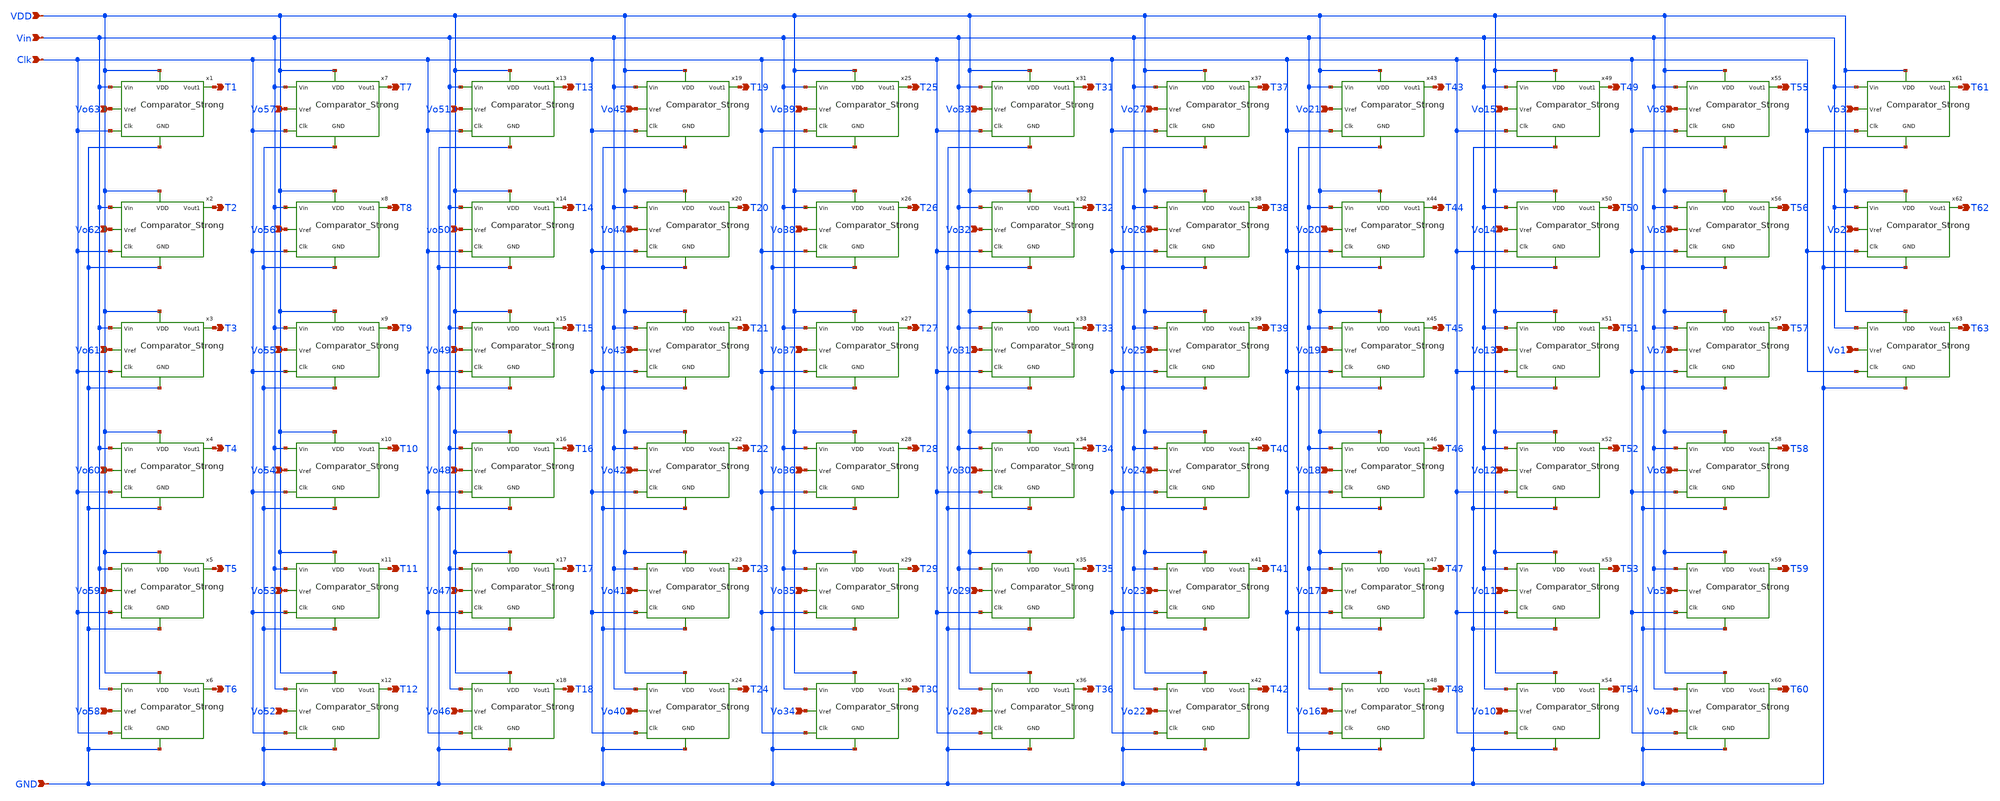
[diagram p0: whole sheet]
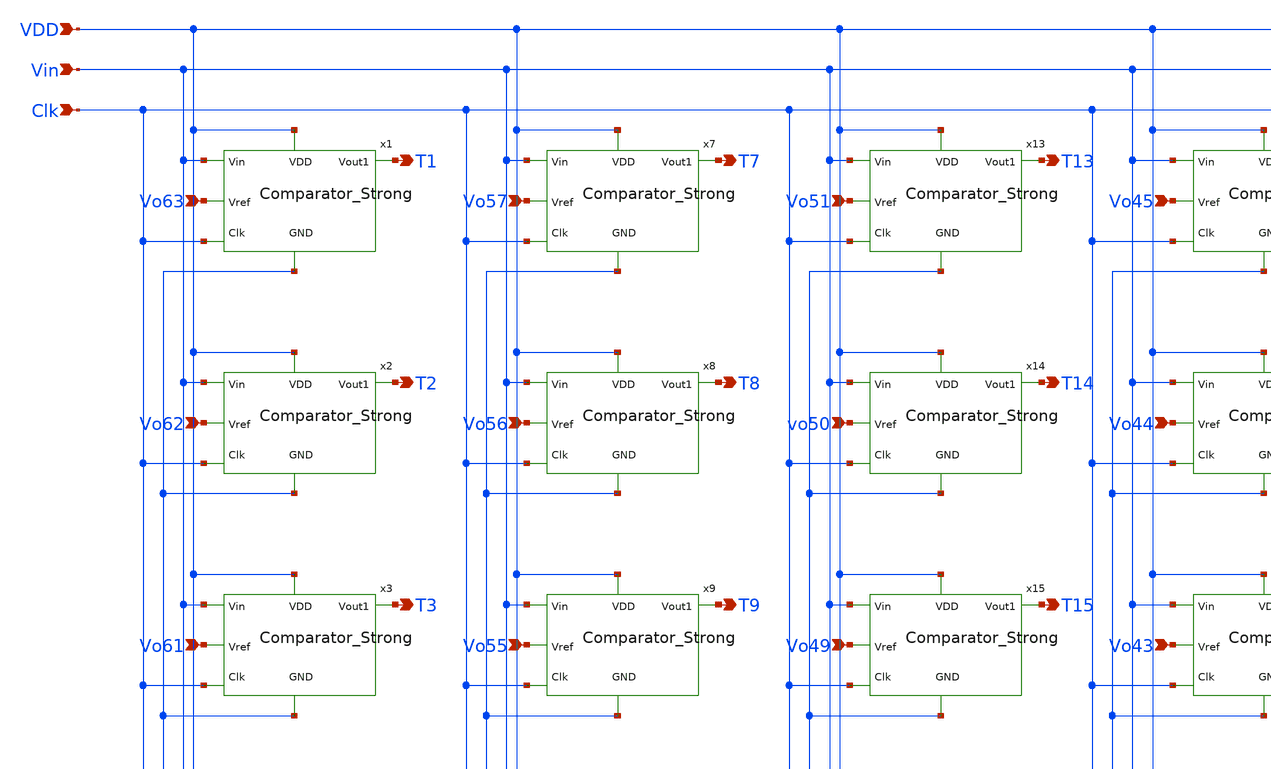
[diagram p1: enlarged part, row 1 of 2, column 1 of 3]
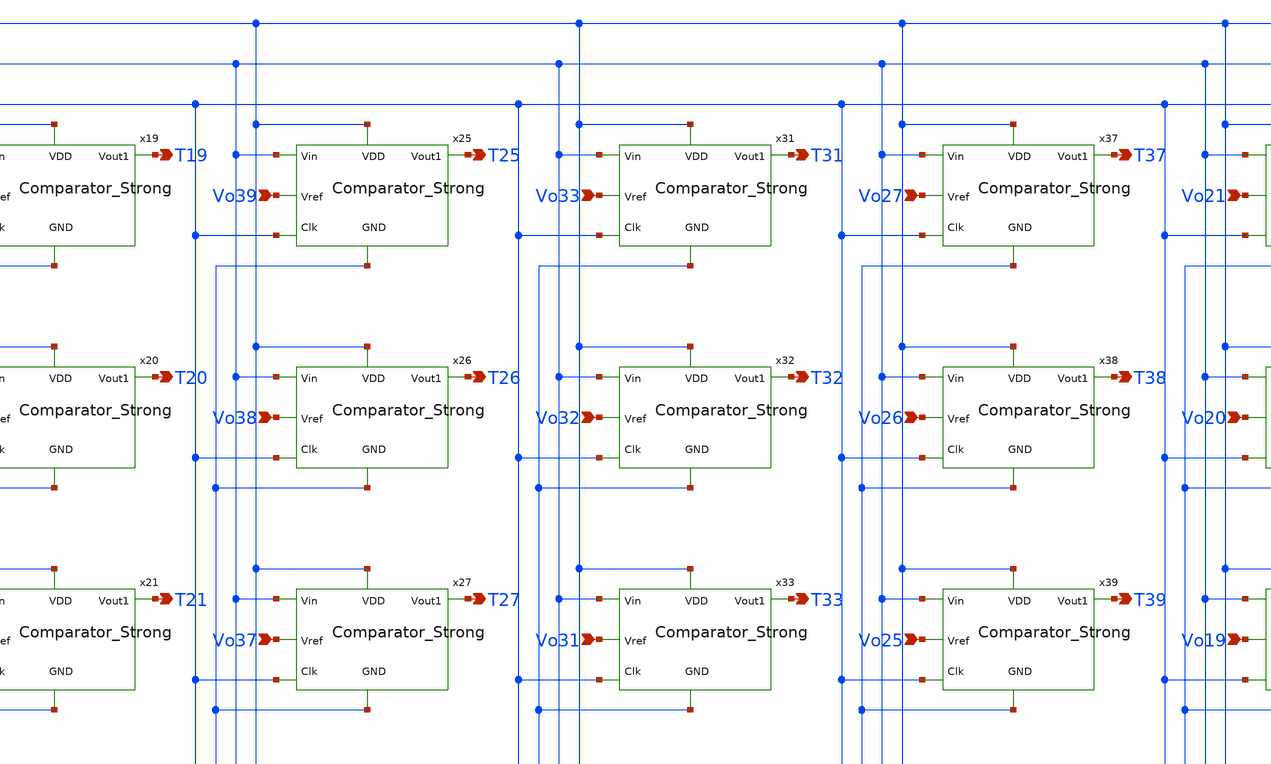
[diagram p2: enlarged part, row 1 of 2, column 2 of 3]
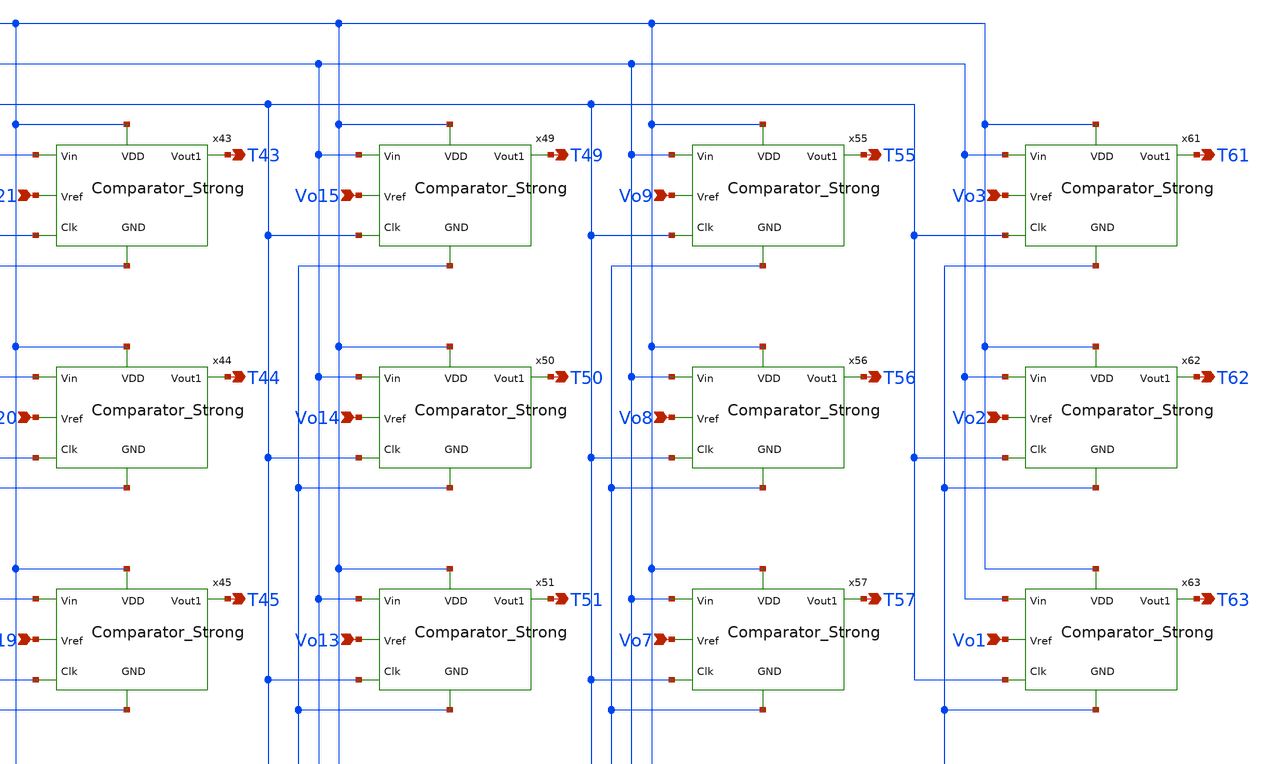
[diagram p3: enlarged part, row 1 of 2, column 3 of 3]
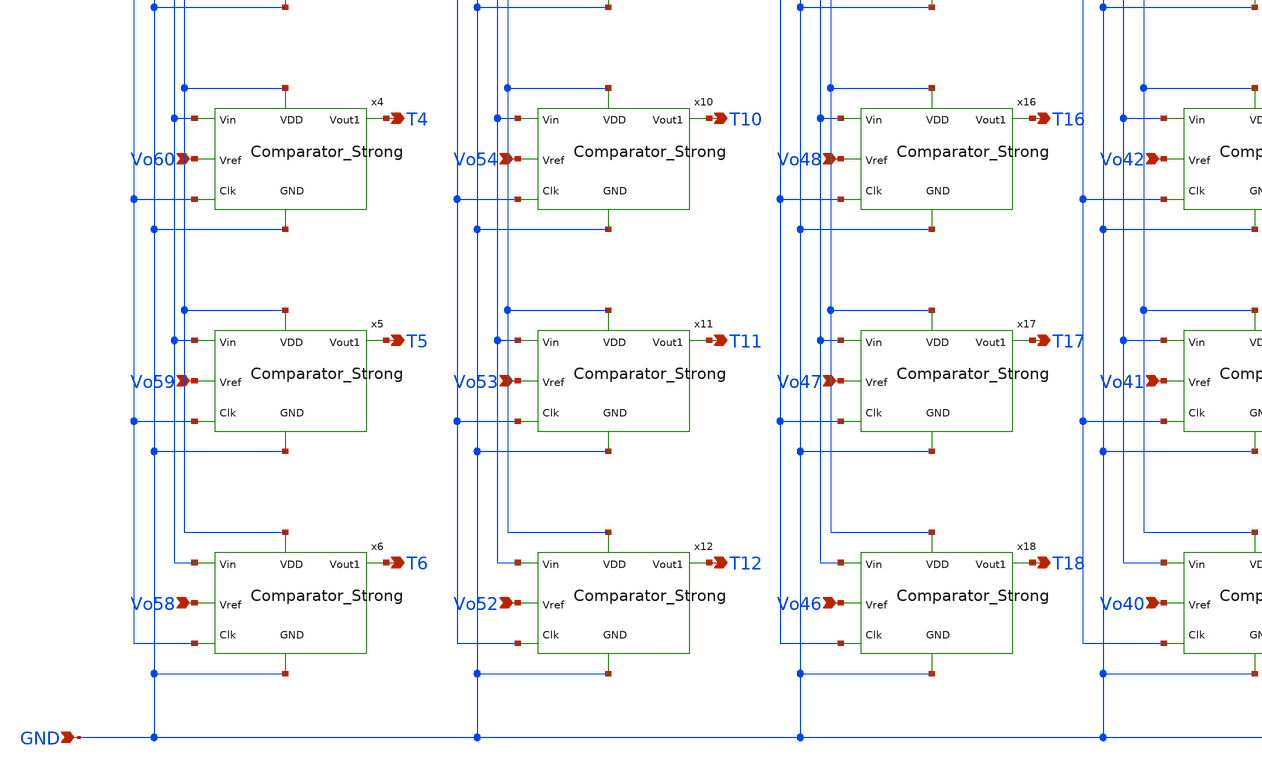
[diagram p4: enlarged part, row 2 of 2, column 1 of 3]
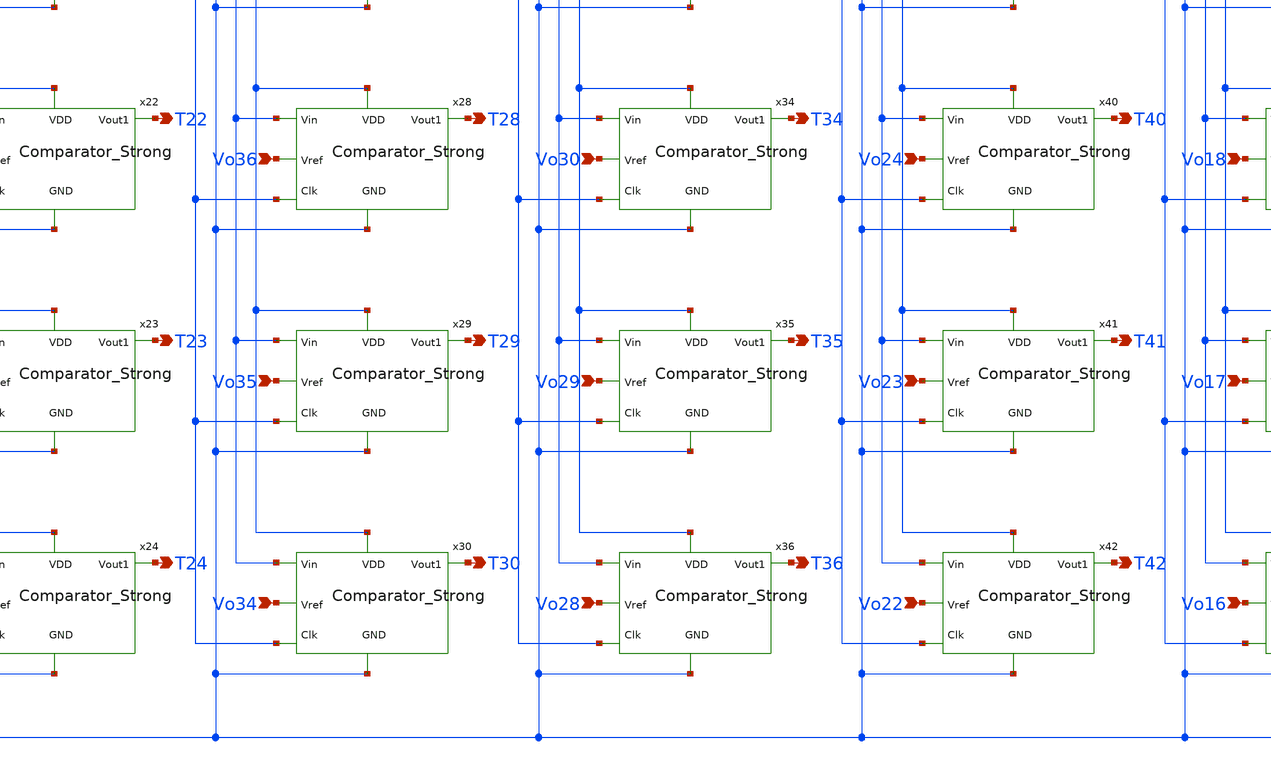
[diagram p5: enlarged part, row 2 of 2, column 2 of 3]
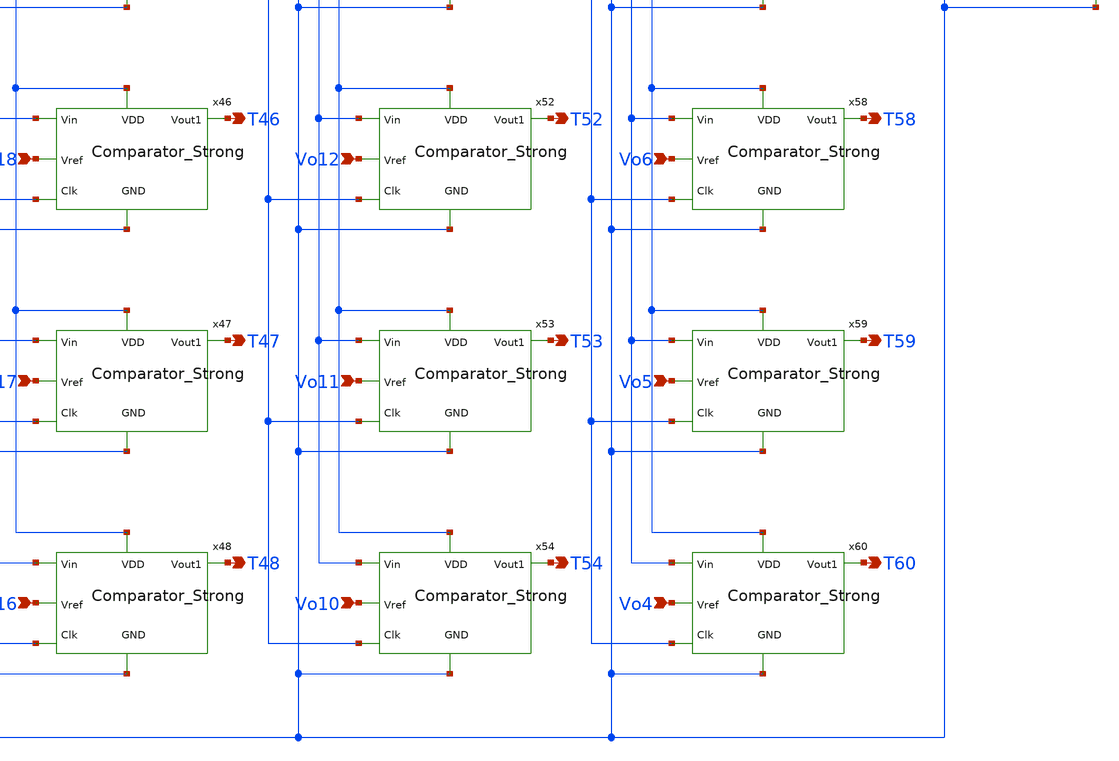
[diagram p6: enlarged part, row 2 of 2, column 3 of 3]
** sch_path: com_64.sch
**.subckt com_64 VDD Vin Clk Vo63 Vo62 Vo61 Vo60 Vo59 Vo58 Vo52 Vo53 Vo54 Vo55 Vo56 Vo57 Vo51 vo50
*+ Vo49 Vo48 Vo47 Vo46 Vo40 Vo41 Vo42 Vo43 Vo44 Vo45 Vo39 Vo37 Vo36 Vo35 Vo34 Vo28 Vo22 Vo29 Vo23 Vo30 Vo24
*+ Vo31 Vo25 Vo32 Vo26 Vo33 Vo27 Vo21 Vo15 Vo20 Vo14 Vo19 Vo13 Vo18 Vo12 Vo17 Vo11 Vo16 Vo10 Vo4 Vo5 Vo6
*+ Vo7 Vo1 Vo8 Vo2 Vo9 Vo3 T1 T7 T2 T8 T3 T9 T4 T10 T5 T11 T6 T12 T18 T24 T17 T23 T16 T22 T15 T21 T14 T20
*+ T13 T19 T25 T26 T27 T28 T29 T30 T36 T42 T35 T41 T34 T40 T33 T39 T32 T38 T31 T37 T43 T49 T44 T50 T45 T51
*+ T46 T52 T47 T53 T48 T54 T60 T59 T58 T57 T63 T56 T62 T55 T61 Vo38 GND
*.ipin VDD
*.ipin Vin
*.ipin Clk
*.ipin Vo63
*.ipin Vo62
*.ipin Vo61
*.ipin Vo60
*.ipin Vo59
*.ipin Vo58
*.ipin Vo52
*.ipin Vo53
*.ipin Vo54
*.ipin Vo55
*.ipin Vo56
*.ipin Vo57
*.ipin Vo51
*.ipin vo50
*.ipin Vo49
*.ipin Vo48
*.ipin Vo47
*.ipin Vo46
*.ipin Vo40
*.ipin Vo41
*.ipin Vo42
*.ipin Vo43
*.ipin Vo44
*.ipin Vo45
*.ipin Vo39
*.ipin Vo37
*.ipin Vo36
*.ipin Vo35
*.ipin Vo34
*.ipin Vo28
*.ipin Vo22
*.ipin Vo29
*.ipin Vo23
*.ipin Vo30
*.ipin Vo24
*.ipin Vo31
*.ipin Vo25
*.ipin Vo32
*.ipin Vo26
*.ipin Vo33
*.ipin Vo27
*.ipin Vo21
*.ipin Vo15
*.ipin Vo20
*.ipin Vo14
*.ipin Vo19
*.ipin Vo13
*.ipin Vo18
*.ipin Vo12
*.ipin Vo17
*.ipin Vo11
*.ipin Vo16
*.ipin Vo10
*.ipin Vo4
*.ipin Vo5
*.ipin Vo6
*.ipin Vo7
*.ipin Vo1
*.ipin Vo8
*.ipin Vo2
*.ipin Vo9
*.ipin Vo3
*.opin T1
*.opin T7
*.opin T2
*.opin T8
*.opin T3
*.opin T9
*.opin T4
*.opin T10
*.opin T5
*.opin T11
*.opin T6
*.opin T12
*.opin T18
*.opin T24
*.opin T17
*.opin T23
*.opin T16
*.opin T22
*.opin T15
*.opin T21
*.opin T14
*.opin T20
*.opin T13
*.opin T19
*.opin T25
*.opin T26
*.opin T27
*.opin T28
*.opin T29
*.opin T30
*.opin T36
*.opin T42
*.opin T35
*.opin T41
*.opin T34
*.opin T40
*.opin T33
*.opin T39
*.opin T32
*.opin T38
*.opin T31
*.opin T37
*.opin T43
*.opin T49
*.opin T44
*.opin T50
*.opin T45
*.opin T51
*.opin T46
*.opin T52
*.opin T47
*.opin T53
*.opin T48
*.opin T54
*.opin T60
*.opin T59
*.opin T58
*.opin T57
*.opin T63
*.opin T56
*.opin T62
*.opin T55
*.opin T61
*.ipin Vo38
*.ipin GND
x1 VDD Vin T1 Vo63 Clk GND Comparator_Strong
x2 VDD Vin T2 Vo62 Clk GND Comparator_Strong
x3 VDD Vin T3 Vo61 Clk GND Comparator_Strong
x4 VDD Vin T4 Vo60 Clk GND Comparator_Strong
x5 VDD Vin T5 Vo59 Clk GND Comparator_Strong
x6 VDD Vin T6 Vo58 Clk GND Comparator_Strong
x7 VDD Vin T7 Vo57 Clk GND Comparator_Strong
x8 VDD Vin T8 Vo56 Clk GND Comparator_Strong
x9 VDD Vin T9 Vo55 Clk GND Comparator_Strong
x10 VDD Vin T10 Vo54 Clk GND Comparator_Strong
x11 VDD Vin T11 Vo53 Clk GND Comparator_Strong
x12 VDD Vin T12 Vo52 Clk GND Comparator_Strong
x13 VDD Vin T13 Vo51 Clk GND Comparator_Strong
x14 VDD Vin T14 vo50 Clk GND Comparator_Strong
x15 VDD Vin T15 Vo49 Clk GND Comparator_Strong
x16 VDD Vin T16 Vo48 Clk GND Comparator_Strong
x17 VDD Vin T17 Vo47 Clk GND Comparator_Strong
x18 VDD Vin T18 Vo46 Clk GND Comparator_Strong
x19 VDD Vin T19 Vo45 Clk GND Comparator_Strong
x20 VDD Vin T20 Vo44 Clk GND Comparator_Strong
x21 VDD Vin T21 Vo43 Clk GND Comparator_Strong
x22 VDD Vin T22 Vo42 Clk GND Comparator_Strong
x23 VDD Vin T23 Vo41 Clk GND Comparator_Strong
x24 VDD Vin T24 Vo40 Clk GND Comparator_Strong
x25 VDD Vin T25 Vo39 Clk GND Comparator_Strong
x26 VDD Vin T26 Vo38 Clk GND Comparator_Strong
x27 VDD Vin T27 Vo37 Clk GND Comparator_Strong
x28 VDD Vin T28 Vo36 Clk GND Comparator_Strong
x29 VDD Vin T29 Vo35 Clk GND Comparator_Strong
x30 VDD Vin T30 Vo34 Clk GND Comparator_Strong
x31 VDD Vin T31 Vo33 Clk GND Comparator_Strong
x32 VDD Vin T32 Vo32 Clk GND Comparator_Strong
x33 VDD Vin T33 Vo31 Clk GND Comparator_Strong
x34 VDD Vin T34 Vo30 Clk GND Comparator_Strong
x35 VDD Vin T35 Vo29 Clk GND Comparator_Strong
x36 VDD Vin T36 Vo28 Clk GND Comparator_Strong
x37 VDD Vin T37 Vo27 Clk GND Comparator_Strong
x38 VDD Vin T38 Vo26 Clk GND Comparator_Strong
x39 VDD Vin T39 Vo25 Clk GND Comparator_Strong
x40 VDD Vin T40 Vo24 Clk GND Comparator_Strong
x41 VDD Vin T41 Vo23 Clk GND Comparator_Strong
x42 VDD Vin T42 Vo22 Clk GND Comparator_Strong
x43 VDD Vin T43 Vo21 Clk GND Comparator_Strong
x44 VDD Vin T44 Vo20 Clk GND Comparator_Strong
x45 VDD Vin T45 Vo19 Clk GND Comparator_Strong
x46 VDD Vin T46 Vo18 Clk GND Comparator_Strong
x47 VDD Vin T47 Vo17 Clk GND Comparator_Strong
x48 VDD Vin T48 Vo16 Clk GND Comparator_Strong
x49 VDD Vin T49 Vo15 Clk GND Comparator_Strong
x50 VDD Vin T50 Vo14 Clk GND Comparator_Strong
x51 VDD Vin T51 Vo13 Clk GND Comparator_Strong
x52 VDD Vin T52 Vo12 Clk GND Comparator_Strong
x53 VDD Vin T53 Vo11 Clk GND Comparator_Strong
x54 VDD Vin T54 Vo10 Clk GND Comparator_Strong
x55 VDD Vin T55 Vo9 Clk GND Comparator_Strong
x56 VDD Vin T56 Vo8 Clk GND Comparator_Strong
x57 VDD Vin T57 Vo7 Clk GND Comparator_Strong
x58 VDD Vin T58 Vo6 Clk GND Comparator_Strong
x59 VDD Vin T59 Vo5 Clk GND Comparator_Strong
x60 VDD Vin T60 Vo4 Clk GND Comparator_Strong
x61 VDD Vin T61 Vo3 Clk GND Comparator_Strong
x62 VDD Vin T62 Vo2 Clk GND Comparator_Strong
x63 VDD Vin T63 Vo1 Clk GND Comparator_Strong
**.ends

* expanding   symbol:  /home/huydq/Comparator_Strong.sym # of pins=6
** sym_path: Comparator_Strong.sym
** sch_path: Comparator_Strong.sch
.subckt Comparator_Strong VDD Vin Vout1 Vref Clk GND
*.ipin Vin
*.ipin Vref
*.ipin Clk
*.ipin GND
*.ipin VDD
*.opin Vout1
x1 VDD net2 net1 Vin Vref Clk GND Strong_arm_latch
x2 net2 net1 VDD GND Vout1 SR_3.3
.ends


* expanding   symbol:  /home/huydq/Strong_arm_latch.sym # of pins=7
** sym_path: Strong_arm_latch.sym
** sch_path: Strong_arm_latch.sch
.subckt Strong_arm_latch VDD Vout2 Vout1 Vin Vref Clk GND
*.ipin Vin
*.ipin Vref
*.ipin Clk
*.ipin VDD
*.opin Vout2
*.opin Vout1
*.ipin GND
XM8 Vout2 Vout1 net2 GND sky130_fd_pr__nfet_g5v0d10v5 L=0.5 W=8 nf=4 ad='int((nf+1)/2) * W/nf * 0.29'
+ as='int((nf+2)/2) * W/nf * 0.29' pd='2*int((nf+1)/2) * (W/nf + 0.29)' ps='2*int((nf+2)/2) * (W/nf + 0.29)'
+ nrd='0.29 / W' nrs='0.29 / W' sa=0 sb=0 sd=0 mult=1 m=1
XM7 Vout1 Vout2 net1 GND sky130_fd_pr__nfet_g5v0d10v5 L=0.5 W=8 nf=4 ad='int((nf+1)/2) * W/nf * 0.29'
+ as='int((nf+2)/2) * W/nf * 0.29' pd='2*int((nf+1)/2) * (W/nf + 0.29)' ps='2*int((nf+2)/2) * (W/nf + 0.29)'
+ nrd='0.29 / W' nrs='0.29 / W' sa=0 sb=0 sd=0 mult=1 m=1
XM10 Vout2 Vout1 VDD VDD sky130_fd_pr__pfet_g5v0d10v5 L=0.5 W=16 nf=8 ad='int((nf+1)/2) * W/nf * 0.29'
+ as='int((nf+2)/2) * W/nf * 0.29' pd='2*int((nf+1)/2) * (W/nf + 0.29)' ps='2*int((nf+2)/2) * (W/nf + 0.29)'
+ nrd='0.29 / W' nrs='0.29 / W' sa=0 sb=0 sd=0 mult=1 m=1
XM1 Vout1 Vout2 VDD VDD sky130_fd_pr__pfet_g5v0d10v5 L=0.5 W=16 nf=8 ad='int((nf+1)/2) * W/nf * 0.29'
+ as='int((nf+2)/2) * W/nf * 0.29' pd='2*int((nf+1)/2) * (W/nf + 0.29)' ps='2*int((nf+2)/2) * (W/nf + 0.29)'
+ nrd='0.29 / W' nrs='0.29 / W' sa=0 sb=0 sd=0 mult=1 m=1
XM2 net1 Clk VDD VDD sky130_fd_pr__pfet_g5v0d10v5 L=0.5 W=2 nf=2 ad='int((nf+1)/2) * W/nf * 0.29' as='int((nf+2)/2) * W/nf * 0.29'
+ pd='2*int((nf+1)/2) * (W/nf + 0.29)' ps='2*int((nf+2)/2) * (W/nf + 0.29)' nrd='0.29 / W' nrs='0.29 / W'
+ sa=0 sb=0 sd=0 mult=1 m=1
XM3 Vout1 Clk VDD VDD sky130_fd_pr__pfet_g5v0d10v5 L=0.5 W=2 nf=2 ad='int((nf+1)/2) * W/nf * 0.29' as='int((nf+2)/2) * W/nf * 0.29'
+ pd='2*int((nf+1)/2) * (W/nf + 0.29)' ps='2*int((nf+2)/2) * (W/nf + 0.29)' nrd='0.29 / W' nrs='0.29 / W'
+ sa=0 sb=0 sd=0 mult=1 m=1
XM4 Vout2 Clk VDD VDD sky130_fd_pr__pfet_g5v0d10v5 L=0.5 W=2 nf=2 ad='int((nf+1)/2) * W/nf * 0.29' as='int((nf+2)/2) * W/nf * 0.29'
+ pd='2*int((nf+1)/2) * (W/nf + 0.29)' ps='2*int((nf+2)/2) * (W/nf + 0.29)' nrd='0.29 / W' nrs='0.29 / W'
+ sa=0 sb=0 sd=0 mult=1 m=1
XM5 net2 Clk VDD VDD sky130_fd_pr__pfet_g5v0d10v5 L=0.5 W=2 nf=2 ad='int((nf+1)/2) * W/nf * 0.29' as='int((nf+2)/2) * W/nf * 0.29'
+ pd='2*int((nf+1)/2) * (W/nf + 0.29)' ps='2*int((nf+2)/2) * (W/nf + 0.29)' nrd='0.29 / W' nrs='0.29 / W'
+ sa=0 sb=0 sd=0 mult=1 m=1
XM6 net1 Vop GND GND sky130_fd_pr__nfet_g5v0d10v5 L=0.5 W=12 nf=6 ad='int((nf+1)/2) * W/nf * 0.29' as='int((nf+2)/2) * W/nf * 0.29'
+ pd='2*int((nf+1)/2) * (W/nf + 0.29)' ps='2*int((nf+2)/2) * (W/nf + 0.29)' nrd='0.29 / W' nrs='0.29 / W'
+ sa=0 sb=0 sd=0 mult=1 m=1
XM9 net2 Von GND GND sky130_fd_pr__nfet_g5v0d10v5 L=0.5 W=12 nf=6 ad='int((nf+1)/2) * W/nf * 0.29' as='int((nf+2)/2) * W/nf * 0.29'
+ pd='2*int((nf+1)/2) * (W/nf + 0.29)' ps='2*int((nf+2)/2) * (W/nf + 0.29)' nrd='0.29 / W' nrs='0.29 / W'
+ sa=0 sb=0 sd=0 mult=1 m=1
XM16 net3 Clk_not VDD VDD sky130_fd_pr__pfet_g5v0d10v5 L=1 W=10 nf=4 ad='int((nf+1)/2) * W/nf * 0.29'
+ as='int((nf+2)/2) * W/nf * 0.29' pd='2*int((nf+1)/2) * (W/nf + 0.29)' ps='2*int((nf+2)/2) * (W/nf + 0.29)'
+ nrd='0.29 / W' nrs='0.29 / W' sa=0 sb=0 sd=0 mult=1 m=1
XM17 Vop Vin net3 VDD sky130_fd_pr__pfet_g5v0d10v5 L=1 W=40 nf=20 ad='int((nf+1)/2) * W/nf * 0.29' as='int((nf+2)/2) * W/nf * 0.29'
+ pd='2*int((nf+1)/2) * (W/nf + 0.29)' ps='2*int((nf+2)/2) * (W/nf + 0.29)' nrd='0.29 / W' nrs='0.29 / W'
+ sa=0 sb=0 sd=0 mult=1 m=1
XM18 Von Vref net3 VDD sky130_fd_pr__pfet_g5v0d10v5 L=1 W=40 nf=20 ad='int((nf+1)/2) * W/nf * 0.29' as='int((nf+2)/2) * W/nf * 0.29'
+ pd='2*int((nf+1)/2) * (W/nf + 0.29)' ps='2*int((nf+2)/2) * (W/nf + 0.29)' nrd='0.29 / W' nrs='0.29 / W'
+ sa=0 sb=0 sd=0 mult=1 m=1
XM19 Vop Clk_not GND GND sky130_fd_pr__nfet_g5v0d10v5 L=0.5 W=2 nf=1 ad='int((nf+1)/2) * W/nf * 0.29'
+ as='int((nf+2)/2) * W/nf * 0.29' pd='2*int((nf+1)/2) * (W/nf + 0.29)' ps='2*int((nf+2)/2) * (W/nf + 0.29)'
+ nrd='0.29 / W' nrs='0.29 / W' sa=0 sb=0 sd=0 mult=1 m=1
XM20 Von Clk_not GND GND sky130_fd_pr__nfet_g5v0d10v5 L=0.5 W=2 nf=1 ad='int((nf+1)/2) * W/nf * 0.29'
+ as='int((nf+2)/2) * W/nf * 0.29' pd='2*int((nf+1)/2) * (W/nf + 0.29)' ps='2*int((nf+2)/2) * (W/nf + 0.29)'
+ nrd='0.29 / W' nrs='0.29 / W' sa=0 sb=0 sd=0 mult=1 m=1
XM11 Clk_not Clk GND GND sky130_fd_pr__nfet_g5v0d10v5 L=0.5 W=4 nf=2 ad='int((nf+1)/2) * W/nf * 0.29'
+ as='int((nf+2)/2) * W/nf * 0.29' pd='2*int((nf+1)/2) * (W/nf + 0.29)' ps='2*int((nf+2)/2) * (W/nf + 0.29)'
+ nrd='0.29 / W' nrs='0.29 / W' sa=0 sb=0 sd=0 mult=1 m=1
XM13 Clk_not Clk VDD VDD sky130_fd_pr__pfet_g5v0d10v5 L=0.5 W=10 nf=4 ad='int((nf+1)/2) * W/nf * 0.29'
+ as='int((nf+2)/2) * W/nf * 0.29' pd='2*int((nf+1)/2) * (W/nf + 0.29)' ps='2*int((nf+2)/2) * (W/nf + 0.29)'
+ nrd='0.29 / W' nrs='0.29 / W' sa=0 sb=0 sd=0 mult=1 m=1
.ends


* expanding   symbol:  /home/huydq/SR_3.3.sym # of pins=5
** sym_path: SR_3.3.sym
** sch_path: SR_3.3.sch
.subckt SR_3.3 Vin2 Vin1 VDD GND Vout1
*.ipin Vin1
*.ipin Vin2
*.ipin VDD
*.ipin GND
*.opin Vout1
XM9 net3 Vin1 GND GND sky130_fd_pr__nfet_g5v0d10v5 L=0.5 W=4 nf=2 ad='int((nf+1)/2) * W/nf * 0.29' as='int((nf+2)/2) * W/nf * 0.29'
+ pd='2*int((nf+1)/2) * (W/nf + 0.29)' ps='2*int((nf+2)/2) * (W/nf + 0.29)' nrd='0.29 / W' nrs='0.29 / W'
+ sa=0 sb=0 sd=0 mult=1 m=1
XM1 Vo1 net3 GND GND sky130_fd_pr__nfet_g5v0d10v5 L=0.5 W=4 nf=2 ad='int((nf+1)/2) * W/nf * 0.29' as='int((nf+2)/2) * W/nf * 0.29'
+ pd='2*int((nf+1)/2) * (W/nf + 0.29)' ps='2*int((nf+2)/2) * (W/nf + 0.29)' nrd='0.29 / W' nrs='0.29 / W'
+ sa=0 sb=0 sd=0 mult=1 m=1
XM2 net1 net2 GND GND sky130_fd_pr__nfet_g5v0d10v5 L=0.5 W=4 nf=2 ad='int((nf+1)/2) * W/nf * 0.29' as='int((nf+2)/2) * W/nf * 0.29'
+ pd='2*int((nf+1)/2) * (W/nf + 0.29)' ps='2*int((nf+2)/2) * (W/nf + 0.29)' nrd='0.29 / W' nrs='0.29 / W'
+ sa=0 sb=0 sd=0 mult=1 m=1
XM3 net2 Vin2 GND GND sky130_fd_pr__nfet_g5v0d10v5 L=0.5 W=4 nf=2 ad='int((nf+1)/2) * W/nf * 0.29' as='int((nf+2)/2) * W/nf * 0.29'
+ pd='2*int((nf+1)/2) * (W/nf + 0.29)' ps='2*int((nf+2)/2) * (W/nf + 0.29)' nrd='0.29 / W' nrs='0.29 / W'
+ sa=0 sb=0 sd=0 mult=1 m=1
XM4 net3 Vin1 VDD VDD sky130_fd_pr__pfet_g5v0d10v5 L=0.5 W=8 nf=4 ad='int((nf+1)/2) * W/nf * 0.29' as='int((nf+2)/2) * W/nf * 0.29'
+ pd='2*int((nf+1)/2) * (W/nf + 0.29)' ps='2*int((nf+2)/2) * (W/nf + 0.29)' nrd='0.29 / W' nrs='0.29 / W'
+ sa=0 sb=0 sd=0 mult=1 m=1
XM5 net1 Vo1 VDD VDD sky130_fd_pr__pfet_g5v0d10v5 L=0.5 W=8 nf=4 ad='int((nf+1)/2) * W/nf * 0.29' as='int((nf+2)/2) * W/nf * 0.29'
+ pd='2*int((nf+1)/2) * (W/nf + 0.29)' ps='2*int((nf+2)/2) * (W/nf + 0.29)' nrd='0.29 / W' nrs='0.29 / W'
+ sa=0 sb=0 sd=0 mult=1 m=1
XM6 Vo1 net1 VDD VDD sky130_fd_pr__pfet_g5v0d10v5 L=0.5 W=8 nf=4 ad='int((nf+1)/2) * W/nf * 0.29' as='int((nf+2)/2) * W/nf * 0.29'
+ pd='2*int((nf+1)/2) * (W/nf + 0.29)' ps='2*int((nf+2)/2) * (W/nf + 0.29)' nrd='0.29 / W' nrs='0.29 / W'
+ sa=0 sb=0 sd=0 mult=1 m=1
XM7 net2 Vin2 VDD VDD sky130_fd_pr__pfet_g5v0d10v5 L=0.5 W=8 nf=4 ad='int((nf+1)/2) * W/nf * 0.29' as='int((nf+2)/2) * W/nf * 0.29'
+ pd='2*int((nf+1)/2) * (W/nf + 0.29)' ps='2*int((nf+2)/2) * (W/nf + 0.29)' nrd='0.29 / W' nrs='0.29 / W'
+ sa=0 sb=0 sd=0 mult=1 m=1
XM8 Vout1 net4 GND GND sky130_fd_pr__nfet_g5v0d10v5 L=0.5 W=8 nf=4 ad='int((nf+1)/2) * W/nf * 0.29' as='int((nf+2)/2) * W/nf * 0.29'
+ pd='2*int((nf+1)/2) * (W/nf + 0.29)' ps='2*int((nf+2)/2) * (W/nf + 0.29)' nrd='0.29 / W' nrs='0.29 / W'
+ sa=0 sb=0 sd=0 mult=1 m=1
XM10 Vout1 net4 VDD VDD sky130_fd_pr__pfet_g5v0d10v5 L=0.5 W=16 nf=8 ad='int((nf+1)/2) * W/nf * 0.29'
+ as='int((nf+2)/2) * W/nf * 0.29' pd='2*int((nf+1)/2) * (W/nf + 0.29)' ps='2*int((nf+2)/2) * (W/nf + 0.29)'
+ nrd='0.29 / W' nrs='0.29 / W' sa=0 sb=0 sd=0 mult=1 m=1
XM11 net4 Vo1 GND GND sky130_fd_pr__nfet_g5v0d10v5 L=0.5 W=2 nf=1 ad='int((nf+1)/2) * W/nf * 0.29' as='int((nf+2)/2) * W/nf * 0.29'
+ pd='2*int((nf+1)/2) * (W/nf + 0.29)' ps='2*int((nf+2)/2) * (W/nf + 0.29)' nrd='0.29 / W' nrs='0.29 / W'
+ sa=0 sb=0 sd=0 mult=1 m=1
XM12 net4 Vo1 VDD VDD sky130_fd_pr__pfet_g5v0d10v5 L=0.5 W=4 nf=2 ad='int((nf+1)/2) * W/nf * 0.29' as='int((nf+2)/2) * W/nf * 0.29'
+ pd='2*int((nf+1)/2) * (W/nf + 0.29)' ps='2*int((nf+2)/2) * (W/nf + 0.29)' nrd='0.29 / W' nrs='0.29 / W'
+ sa=0 sb=0 sd=0 mult=1 m=1
.ends

.end
